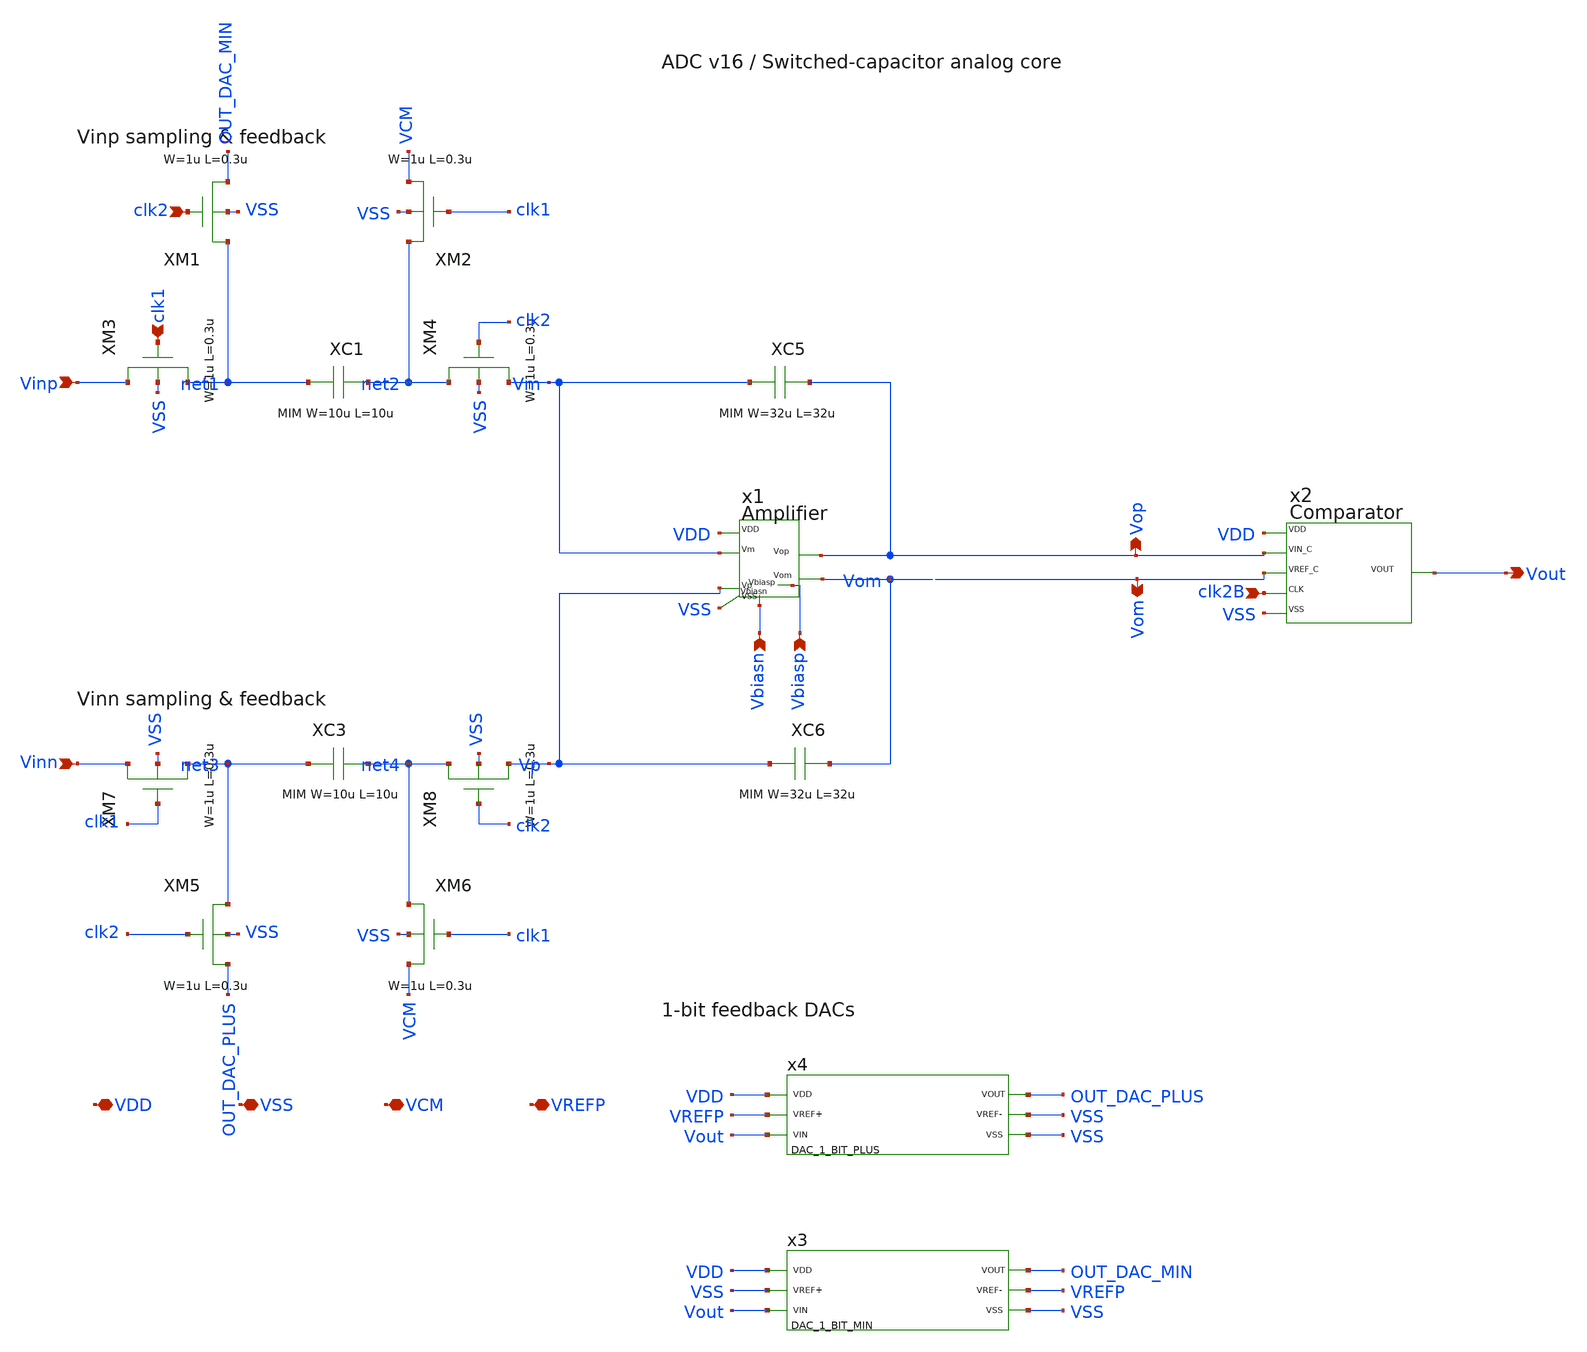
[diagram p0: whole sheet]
** sch_path: src/schematics/INTEGRATION/ADC_final/ADC_v17_Xschem/analog_integration_lvs.sch
* Copyright (C) 1998-2026 Stefan Frederik Schippers
* This program is free software; you can redistribute it and/or modify
* it under the terms of the GNU General Public License as published by
* the Free Software Foundation; either version 2 of the License, or
* (at your option) any later version.
**.subckt analog_integration_lvs Vinp Vinn Vop Vom clk1 clk2 Vbiasn Vbiasp clk2B Vout VDD VSS VCM
*+ VREFP
*.ipin Vinp
*.ipin Vinn
*.opin Vop
*.opin Vom
*.ipin clk1
*.ipin clk2
*.ipin Vbiasn
*.ipin Vbiasp
*.ipin clk2B
*.opin Vout
*.iopin VDD
*.iopin VSS
*.iopin VCM
*.iopin VREFP
XM1 net1 clk2 OUT_DAC_MIN VSS nfet_03v3 L=0.3u W=1u nf=1 ad='int((nf+1)/2) * W/nf * 0.18u' as='int((nf+2)/2) * W/nf * 0.18u'
+ pd='2*int((nf+1)/2) * (W/nf + 0.18u)' ps='2*int((nf+2)/2) * (W/nf + 0.18u)' nrd='0.18u / W' nrs='0.18u / W'
+ sa=0 sb=0 sd=0
XM2 net2 clk1 VCM VSS nfet_03v3 L=0.3u W=1u nf=1 ad='int((nf+1)/2) * W/nf * 0.18u' as='int((nf+2)/2) * W/nf * 0.18u'
+ pd='2*int((nf+1)/2) * (W/nf + 0.18u)' ps='2*int((nf+2)/2) * (W/nf + 0.18u)' nrd='0.18u / W' nrs='0.18u / W'
+ sa=0 sb=0 sd=0
XM3 Vinp clk1 net1 VSS nfet_03v3 L=0.3u W=1u nf=1 ad='int((nf+1)/2) * W/nf * 0.18u' as='int((nf+2)/2) * W/nf * 0.18u'
+ pd='2*int((nf+1)/2) * (W/nf + 0.18u)' ps='2*int((nf+2)/2) * (W/nf + 0.18u)' nrd='0.18u / W' nrs='0.18u / W'
+ sa=0 sb=0 sd=0
XM4 net2 clk2 Vm VSS nfet_03v3 L=0.3u W=1u nf=1 ad='int((nf+1)/2) * W/nf * 0.18u' as='int((nf+2)/2) * W/nf * 0.18u'
+ pd='2*int((nf+1)/2) * (W/nf + 0.18u)' ps='2*int((nf+2)/2) * (W/nf + 0.18u)' nrd='0.18u / W' nrs='0.18u / W'
+ sa=0 sb=0 sd=0
XM5 net3 clk2 OUT_DAC_PLUS VSS nfet_03v3 L=0.3u W=1u nf=1 ad='int((nf+1)/2) * W/nf * 0.18u' as='int((nf+2)/2) * W/nf * 0.18u'
+ pd='2*int((nf+1)/2) * (W/nf + 0.18u)' ps='2*int((nf+2)/2) * (W/nf + 0.18u)' nrd='0.18u / W' nrs='0.18u / W'
+ sa=0 sb=0 sd=0
XM6 net4 clk1 VCM VSS nfet_03v3 L=0.3u W=1u nf=1 ad='int((nf+1)/2) * W/nf * 0.18u' as='int((nf+2)/2) * W/nf * 0.18u'
+ pd='2*int((nf+1)/2) * (W/nf + 0.18u)' ps='2*int((nf+2)/2) * (W/nf + 0.18u)' nrd='0.18u / W' nrs='0.18u / W'
+ sa=0 sb=0 sd=0
XM7 Vinn clk1 net3 VSS nfet_03v3 L=0.3u W=1u nf=1 ad='int((nf+1)/2) * W/nf * 0.18u' as='int((nf+2)/2) * W/nf * 0.18u'
+ pd='2*int((nf+1)/2) * (W/nf + 0.18u)' ps='2*int((nf+2)/2) * (W/nf + 0.18u)' nrd='0.18u / W' nrs='0.18u / W'
+ sa=0 sb=0 sd=0
XM8 net4 clk2 Vp VSS nfet_03v3 L=0.3u W=1u nf=1 ad='int((nf+1)/2) * W/nf * 0.18u' as='int((nf+2)/2) * W/nf * 0.18u'
+ pd='2*int((nf+1)/2) * (W/nf + 0.18u)' ps='2*int((nf+2)/2) * (W/nf + 0.18u)' nrd='0.18u / W' nrs='0.18u / W'
+ sa=0 sb=0 sd=0
XC1 net2 net1 cap_mim_2f0_m4m5_noshield c_width=10u c_length=10u
XC3 net3 net4 cap_mim_2f0_m4m5_noshield c_width=10u c_length=10u
XC5 Vop Vm cap_mim_2f0_m4m5_noshield c_width=32u c_length=32u
XC6 Vom Vp cap_mim_2f0_m4m5_noshield c_width=32u c_length=32u
x1 VDD Vbiasp Vp Vop Vm Vom Vbiasn VSS fulldiffamp
x2 VDD Vop Vom clk2B Vout VSS ADCv16_verified_comparator
x4 VDD VREFP Vout OUT_DAC_PLUS VSS VSS DAC_1_BIT_PLUS
x3 VDD VSS Vout OUT_DAC_MIN VREFP VSS DAC_1_BIT_MIN
**.ends

* expanding   symbol:  ./fulldiffamp.sym # of pins=8
** sym_path: ./fulldiffamp.sym
** sch_path: ./fulldiffamp.sch
.subckt fulldiffamp VDD Vbiasp Vp Vop Vm Vom Vbiasn VSS
*.iopin VDD
*.iopin Vbiasp
*.iopin Vp
*.iopin Vop
*.iopin Vm
*.iopin Vom
*.iopin Vbiasn
*.iopin VSS
XM5 net2 Vom VDD VDD pfet_03v3 L=2u W=1u nf=1 ad='int((nf+1)/2) * W/nf * 0.18u' as='int((nf+2)/2) * W/nf * 0.18u'
+ pd='2*int((nf+1)/2) * (W/nf + 0.18u)' ps='2*int((nf+2)/2) * (W/nf + 0.18u)' nrd='0.18u / W' nrs='0.18u / W'
+ sa=0 sb=0 sd=0
XM2 Vom Vbiasp VDD VDD pfet_03v3 L=5u W=10u nf=1 ad='int((nf+1)/2) * W/nf * 0.18u' as='int((nf+2)/2) * W/nf * 0.18u'
+ pd='2*int((nf+1)/2) * (W/nf + 0.18u)' ps='2*int((nf+2)/2) * (W/nf + 0.18u)' nrd='0.18u / W' nrs='0.18u / W'
+ sa=0 sb=0 sd=0
XM8 Vom Vm net1 VSS nfet_03v3 L=5u W=10u nf=1 ad='int((nf+1)/2) * W/nf * 0.18u' as='int((nf+2)/2) * W/nf * 0.18u'
+ pd='2*int((nf+1)/2) * (W/nf + 0.18u)' ps='2*int((nf+2)/2) * (W/nf + 0.18u)' nrd='0.18u / W' nrs='0.18u / W'
+ sa=0 sb=0 sd=0
XM7 Vop Vp net1 VSS nfet_03v3 L=5u W=10u nf=1 ad='int((nf+1)/2) * W/nf * 0.18u' as='int((nf+2)/2) * W/nf * 0.18u'
+ pd='2*int((nf+1)/2) * (W/nf + 0.18u)' ps='2*int((nf+2)/2) * (W/nf + 0.18u)' nrd='0.18u / W' nrs='0.18u / W'
+ sa=0 sb=0 sd=0
XM1 Vop Vbiasp VDD VDD pfet_03v3 L=5u W=10u nf=1 ad='int((nf+1)/2) * W/nf * 0.18u' as='int((nf+2)/2) * W/nf * 0.18u'
+ pd='2*int((nf+1)/2) * (W/nf + 0.18u)' ps='2*int((nf+2)/2) * (W/nf + 0.18u)' nrd='0.18u / W' nrs='0.18u / W'
+ sa=0 sb=0 sd=0
XM6 net3 Vop VDD VDD pfet_03v3 L=2u W=1u nf=1 ad='int((nf+1)/2) * W/nf * 0.18u' as='int((nf+2)/2) * W/nf * 0.18u'
+ pd='2*int((nf+1)/2) * (W/nf + 0.18u)' ps='2*int((nf+2)/2) * (W/nf + 0.18u)' nrd='0.18u / W' nrs='0.18u / W'
+ sa=0 sb=0 sd=0
XM4 Vom VDD VDD VDD pfet_03v3 L=5u W=0.5u nf=1 ad='int((nf+1)/2) * W/nf * 0.18u' as='int((nf+2)/2) * W/nf * 0.18u'
+ pd='2*int((nf+1)/2) * (W/nf + 0.18u)' ps='2*int((nf+2)/2) * (W/nf + 0.18u)' nrd='0.18u / W' nrs='0.18u / W'
+ sa=0 sb=0 sd=0
XM3 Vop VDD VDD VDD pfet_03v3 L=5u W=0.5u nf=1 ad='int((nf+1)/2) * W/nf * 0.18u' as='int((nf+2)/2) * W/nf * 0.18u'
+ pd='2*int((nf+1)/2) * (W/nf + 0.18u)' ps='2*int((nf+2)/2) * (W/nf + 0.18u)' nrd='0.18u / W' nrs='0.18u / W'
+ sa=0 sb=0 sd=0
XM9 net1 Vbiasn VSS VSS nfet_03v3 L=2u W=10u nf=1 ad='int((nf+1)/2) * W/nf * 0.18u' as='int((nf+2)/2) * W/nf * 0.18u'
+ pd='2*int((nf+1)/2) * (W/nf + 0.18u)' ps='2*int((nf+2)/2) * (W/nf + 0.18u)' nrd='0.18u / W' nrs='0.18u / W'
+ sa=0 sb=0 sd=0
XM10 net1 Vbiasn VSS VSS nfet_03v3 L=2u W=10u nf=1 ad='int((nf+1)/2) * W/nf * 0.18u' as='int((nf+2)/2) * W/nf * 0.18u'
+ pd='2*int((nf+1)/2) * (W/nf + 0.18u)' ps='2*int((nf+2)/2) * (W/nf + 0.18u)' nrd='0.18u / W' nrs='0.18u / W'
+ sa=0 sb=0 sd=0
XM11 Vop net2 VSS VSS nfet_03v3 L=15u W=0.5u nf=1 ad='int((nf+1)/2) * W/nf * 0.18u' as='int((nf+2)/2) * W/nf * 0.18u'
+ pd='2*int((nf+1)/2) * (W/nf + 0.18u)' ps='2*int((nf+2)/2) * (W/nf + 0.18u)' nrd='0.18u / W' nrs='0.18u / W'
+ sa=0 sb=0 sd=0
XM13 net2 net2 VSS VSS nfet_03v3 L=0.35u W=5u nf=1 ad='int((nf+1)/2) * W/nf * 0.18u' as='int((nf+2)/2) * W/nf * 0.18u'
+ pd='2*int((nf+1)/2) * (W/nf + 0.18u)' ps='2*int((nf+2)/2) * (W/nf + 0.18u)' nrd='0.18u / W' nrs='0.18u / W'
+ sa=0 sb=0 sd=0
XM12 net3 net3 VSS VSS nfet_03v3 L=0.35u W=5u nf=1 ad='int((nf+1)/2) * W/nf * 0.18u' as='int((nf+2)/2) * W/nf * 0.18u'
+ pd='2*int((nf+1)/2) * (W/nf + 0.18u)' ps='2*int((nf+2)/2) * (W/nf + 0.18u)' nrd='0.18u / W' nrs='0.18u / W'
+ sa=0 sb=0 sd=0
XM14 Vom net3 VSS VSS nfet_03v3 L=15u W=0.5u nf=1 ad='int((nf+1)/2) * W/nf * 0.18u' as='int((nf+2)/2) * W/nf * 0.18u'
+ pd='2*int((nf+1)/2) * (W/nf + 0.18u)' ps='2*int((nf+2)/2) * (W/nf + 0.18u)' nrd='0.18u / W' nrs='0.18u / W'
+ sa=0 sb=0 sd=0
.ends


* expanding   symbol:  ./ADCv16_verified_comparator.sym # of pins=6
** sym_path: ./ADCv16_verified_comparator.sym
** sch_path: ./ADCv16_verified_comparator.sch
.subckt ADCv16_verified_comparator VDD VIN_C VREF_C CLK VOUT VSS
*.iopin VDD
*.iopin VIN_C
*.iopin VREF_C
*.iopin CLK
*.iopin VOUT
*.iopin VSS
XM1 net3 VIN_C net1 VDD pfet_03v3 L=0.3u W=5u nf=1 ad='int((nf+1)/2) * W/nf * 0.18u' as='int((nf+2)/2) * W/nf * 0.18u'
+ pd='2*int((nf+1)/2) * (W/nf + 0.18u)' ps='2*int((nf+2)/2) * (W/nf + 0.18u)' nrd='0.18u / W' nrs='0.18u / W'
+ sa=0 sb=0 sd=0
XM2 net5 VREF_C net1 VDD pfet_03v3 L=0.3u W=5u nf=1 ad='int((nf+1)/2) * W/nf * 0.18u' as='int((nf+2)/2) * W/nf * 0.18u'
+ pd='2*int((nf+1)/2) * (W/nf + 0.18u)' ps='2*int((nf+2)/2) * (W/nf + 0.18u)' nrd='0.18u / W' nrs='0.18u / W'
+ sa=0 sb=0 sd=0
XM3 VOUT net2 net5 VDD pfet_03v3 L=0.3u W=5u nf=1 ad='int((nf+1)/2) * W/nf * 0.18u' as='int((nf+2)/2) * W/nf * 0.18u'
+ pd='2*int((nf+1)/2) * (W/nf + 0.18u)' ps='2*int((nf+2)/2) * (W/nf + 0.18u)' nrd='0.18u / W' nrs='0.18u / W'
+ sa=0 sb=0 sd=0
XM4 net4 net2 net3 VDD pfet_03v3 L=0.3u W=5u nf=1 ad='int((nf+1)/2) * W/nf * 0.18u' as='int((nf+2)/2) * W/nf * 0.18u'
+ pd='2*int((nf+1)/2) * (W/nf + 0.18u)' ps='2*int((nf+2)/2) * (W/nf + 0.18u)' nrd='0.18u / W' nrs='0.18u / W'
+ sa=0 sb=0 sd=0
XM6 net2 CLK VDD VDD pfet_03v3 L=0.3u W=5u nf=1 ad='int((nf+1)/2) * W/nf * 0.18u' as='int((nf+2)/2) * W/nf * 0.18u'
+ pd='2*int((nf+1)/2) * (W/nf + 0.18u)' ps='2*int((nf+2)/2) * (W/nf + 0.18u)' nrd='0.18u / W' nrs='0.18u / W'
+ sa=0 sb=0 sd=0
XM7 net2 CLK VSS VSS nfet_03v3 L=0.3u W=2.5u nf=1 ad='int((nf+1)/2) * W/nf * 0.18u' as='int((nf+2)/2) * W/nf * 0.18u'
+ pd='2*int((nf+1)/2) * (W/nf + 0.18u)' ps='2*int((nf+2)/2) * (W/nf + 0.18u)' nrd='0.18u / W' nrs='0.18u / W'
+ sa=0 sb=0 sd=0
XM8 net4 CLK VOUT VSS nfet_03v3 L=0.3u W=2.5u nf=1 ad='int((nf+1)/2) * W/nf * 0.18u' as='int((nf+2)/2) * W/nf * 0.18u'
+ pd='2*int((nf+1)/2) * (W/nf + 0.18u)' ps='2*int((nf+2)/2) * (W/nf + 0.18u)' nrd='0.18u / W' nrs='0.18u / W'
+ sa=0 sb=0 sd=0
XM9 net7 VOUT VDD VDD pfet_03v3 L=0.3u W=5u nf=1 ad='int((nf+1)/2) * W/nf * 0.18u' as='int((nf+2)/2) * W/nf * 0.18u'
+ pd='2*int((nf+1)/2) * (W/nf + 0.18u)' ps='2*int((nf+2)/2) * (W/nf + 0.18u)' nrd='0.18u / W' nrs='0.18u / W'
+ sa=0 sb=0 sd=0
XM10 net4 CLK net7 VDD pfet_03v3 L=0.3u W=5u nf=1 ad='int((nf+1)/2) * W/nf * 0.18u' as='int((nf+2)/2) * W/nf * 0.18u'
+ pd='2*int((nf+1)/2) * (W/nf + 0.18u)' ps='2*int((nf+2)/2) * (W/nf + 0.18u)' nrd='0.18u / W' nrs='0.18u / W'
+ sa=0 sb=0 sd=0
XM11 net4 VOUT VSS VSS nfet_03v3 L=0.3u W=2.5u nf=1 ad='int((nf+1)/2) * W/nf * 0.18u' as='int((nf+2)/2) * W/nf * 0.18u'
+ pd='2*int((nf+1)/2) * (W/nf + 0.18u)' ps='2*int((nf+2)/2) * (W/nf + 0.18u)' nrd='0.18u / W' nrs='0.18u / W'
+ sa=0 sb=0 sd=0
XM12 net6 net4 VDD VDD pfet_03v3 L=0.3u W=5u nf=1 ad='int((nf+1)/2) * W/nf * 0.18u' as='int((nf+2)/2) * W/nf * 0.18u'
+ pd='2*int((nf+1)/2) * (W/nf + 0.18u)' ps='2*int((nf+2)/2) * (W/nf + 0.18u)' nrd='0.18u / W' nrs='0.18u / W'
+ sa=0 sb=0 sd=0
XM13 VOUT CLK net6 VDD pfet_03v3 L=0.3u W=5u nf=1 ad='int((nf+1)/2) * W/nf * 0.18u' as='int((nf+2)/2) * W/nf * 0.18u'
+ pd='2*int((nf+1)/2) * (W/nf + 0.18u)' ps='2*int((nf+2)/2) * (W/nf + 0.18u)' nrd='0.18u / W' nrs='0.18u / W'
+ sa=0 sb=0 sd=0
XM14 VOUT net4 VSS VSS nfet_03v3 L=0.3u W=2.5u nf=1 ad='int((nf+1)/2) * W/nf * 0.18u' as='int((nf+2)/2) * W/nf * 0.18u'
+ pd='2*int((nf+1)/2) * (W/nf + 0.18u)' ps='2*int((nf+2)/2) * (W/nf + 0.18u)' nrd='0.18u / W' nrs='0.18u / W'
+ sa=0 sb=0 sd=0
XM5 net1 VSS VDD VDD pfet_03v3 L=0.3u W=10u nf=1 ad='int((nf+1)/2) * W/nf * 0.18u' as='int((nf+2)/2) * W/nf * 0.18u'
+ pd='2*int((nf+1)/2) * (W/nf + 0.18u)' ps='2*int((nf+2)/2) * (W/nf + 0.18u)' nrd='0.18u / W' nrs='0.18u / W'
+ sa=0 sb=0 sd=0
.ends


* expanding   symbol:  ./DAC_1_BIT_PLUS.sym # of pins=6
** sym_path: ./DAC_1_BIT_PLUS.sym
** sch_path: ./DAC_1_BIT_PLUS.sch
.subckt DAC_1_BIT_PLUS VDD VREF+ VIN VOUT VREF- VSS
*.iopin VDD
*.iopin VREF+
*.iopin VIN
*.iopin VOUT
*.iopin VREF-
*.iopin VSS
XM1 net1 net2 VREF+ VSS nfet_03v3 L=Ld W=Wdn_p nf=2 ad='int((nf+1)/2) * W/nf * 0.18u' as='int((nf+2)/2) * W/nf * 0.18u'
+ pd='2*int((nf+1)/2) * (W/nf + 0.18u)' ps='2*int((nf+2)/2) * (W/nf + 0.18u)' nrd='0.18u / W' nrs='0.18u / W'
+ sa=0 sb=0 sd=0
XM2 net1 VIN VREF+ VDD pfet_03v3 L=Ld W=Wdp_p nf=2 ad='int((nf+1)/2) * W/nf * 0.18u' as='int((nf+2)/2) * W/nf * 0.18u'
+ pd='2*int((nf+1)/2) * (W/nf + 0.18u)' ps='2*int((nf+2)/2) * (W/nf + 0.18u)' nrd='0.18u / W' nrs='0.18u / W'
+ sa=0 sb=0 sd=0
XM3 net1 VIN VREF- VSS nfet_03v3 L=Ld W=Wdn_p nf=2 ad='int((nf+1)/2) * W/nf * 0.18u' as='int((nf+2)/2) * W/nf * 0.18u'
+ pd='2*int((nf+1)/2) * (W/nf + 0.18u)' ps='2*int((nf+2)/2) * (W/nf + 0.18u)' nrd='0.18u / W' nrs='0.18u / W'
+ sa=0 sb=0 sd=0
XM4 net1 net2 VREF- VDD pfet_03v3 L=Ld W=Wdp_p nf=2 ad='int((nf+1)/2) * W/nf * 0.18u' as='int((nf+2)/2) * W/nf * 0.18u'
+ pd='2*int((nf+1)/2) * (W/nf + 0.18u)' ps='2*int((nf+2)/2) * (W/nf + 0.18u)' nrd='0.18u / W' nrs='0.18u / W'
+ sa=0 sb=0 sd=0
XM5 net2 VIN VDD VDD pfet_03v3 L=Ld W=Wsp_p nf=1 ad='int((nf+1)/2) * W/nf * 0.18u' as='int((nf+2)/2) * W/nf * 0.18u'
+ pd='2*int((nf+1)/2) * (W/nf + 0.18u)' ps='2*int((nf+2)/2) * (W/nf + 0.18u)' nrd='0.18u / W' nrs='0.18u / W'
+ sa=0 sb=0 sd=0
XM6 net2 VIN VSS VSS nfet_03v3 L=Ld W=Wsn_p nf=1 ad='int((nf+1)/2) * W/nf * 0.18u' as='int((nf+2)/2) * W/nf * 0.18u'
+ pd='2*int((nf+1)/2) * (W/nf + 0.18u)' ps='2*int((nf+2)/2) * (W/nf + 0.18u)' nrd='0.18u / W' nrs='0.18u / W'
+ sa=0 sb=0 sd=0
XM7 net3 net1 VDD VDD pfet_03v3 L=Ld W=Wsp_p nf=1 ad='int((nf+1)/2) * W/nf * 0.18u' as='int((nf+2)/2) * W/nf * 0.18u'
+ pd='2*int((nf+1)/2) * (W/nf + 0.18u)' ps='2*int((nf+2)/2) * (W/nf + 0.18u)' nrd='0.18u / W' nrs='0.18u / W'
+ sa=0 sb=0 sd=0
XM8 net3 net1 VSS VSS nfet_03v3 L=Ld W=Wsn_p nf=1 ad='int((nf+1)/2) * W/nf * 0.18u' as='int((nf+2)/2) * W/nf * 0.18u'
+ pd='2*int((nf+1)/2) * (W/nf + 0.18u)' ps='2*int((nf+2)/2) * (W/nf + 0.18u)' nrd='0.18u / W' nrs='0.18u / W'
+ sa=0 sb=0 sd=0
XM9 VOUT net3 VDD VDD pfet_03v3 L=Ld W=Wsp2_p nf=1 ad='int((nf+1)/2) * W/nf * 0.18u' as='int((nf+2)/2) * W/nf * 0.18u'
+ pd='2*int((nf+1)/2) * (W/nf + 0.18u)' ps='2*int((nf+2)/2) * (W/nf + 0.18u)' nrd='0.18u / W' nrs='0.18u / W'
+ sa=0 sb=0 sd=0
XM10 VOUT net3 VSS VSS nfet_03v3 L=Ld W=Wsn2_p nf=1 ad='int((nf+1)/2) * W/nf * 0.18u' as='int((nf+2)/2) * W/nf * 0.18u'
+ pd='2*int((nf+1)/2) * (W/nf + 0.18u)' ps='2*int((nf+2)/2) * (W/nf + 0.18u)' nrd='0.18u / W' nrs='0.18u / W'
+ sa=0 sb=0 sd=0
.ends


* expanding   symbol:  ./DAC_1_BIT_MIN.sym # of pins=6
** sym_path: ./DAC_1_BIT_MIN.sym
** sch_path: ./DAC_1_BIT_MIN.sch
.subckt DAC_1_BIT_MIN VDD VREF+ VIN VOUT VREF- VSS
*.iopin VDD
*.iopin VREF+
*.iopin VIN
*.iopin VOUT
*.iopin VREF-
*.iopin VSS
XM1 net1 net2 VREF+ VSS nfet_03v3 L=0.28u W=1u nf=2 ad='int((nf+1)/2) * W/nf * 0.18u' as='int((nf+2)/2) * W/nf * 0.18u'
+ pd='2*int((nf+1)/2) * (W/nf + 0.18u)' ps='2*int((nf+2)/2) * (W/nf + 0.18u)' nrd='0.18u / W' nrs='0.18u / W'
+ sa=0 sb=0 sd=0
XM2 net1 VIN VREF+ VDD pfet_03v3 L=0.28u W=10u nf=2 ad='int((nf+1)/2) * W/nf * 0.18u' as='int((nf+2)/2) * W/nf * 0.18u'
+ pd='2*int((nf+1)/2) * (W/nf + 0.18u)' ps='2*int((nf+2)/2) * (W/nf + 0.18u)' nrd='0.18u / W' nrs='0.18u / W'
+ sa=0 sb=0 sd=0
XM3 net1 VIN VREF- VSS nfet_03v3 L=0.28u W=1u nf=2 ad='int((nf+1)/2) * W/nf * 0.18u' as='int((nf+2)/2) * W/nf * 0.18u'
+ pd='2*int((nf+1)/2) * (W/nf + 0.18u)' ps='2*int((nf+2)/2) * (W/nf + 0.18u)' nrd='0.18u / W' nrs='0.18u / W'
+ sa=0 sb=0 sd=0
XM4 net1 net2 VREF- VDD pfet_03v3 L=0.28u W=10u nf=2 ad='int((nf+1)/2) * W/nf * 0.18u' as='int((nf+2)/2) * W/nf * 0.18u'
+ pd='2*int((nf+1)/2) * (W/nf + 0.18u)' ps='2*int((nf+2)/2) * (W/nf + 0.18u)' nrd='0.18u / W' nrs='0.18u / W'
+ sa=0 sb=0 sd=0
XM5 net2 VIN VDD VDD pfet_03v3 L=0.28u W=5u nf=1 ad='int((nf+1)/2) * W/nf * 0.18u' as='int((nf+2)/2) * W/nf * 0.18u'
+ pd='2*int((nf+1)/2) * (W/nf + 0.18u)' ps='2*int((nf+2)/2) * (W/nf + 0.18u)' nrd='0.18u / W' nrs='0.18u / W'
+ sa=0 sb=0 sd=0
XM6 net2 VIN VSS VSS nfet_03v3 L=0.28u W=0.5u nf=1 ad='int((nf+1)/2) * W/nf * 0.18u' as='int((nf+2)/2) * W/nf * 0.18u'
+ pd='2*int((nf+1)/2) * (W/nf + 0.18u)' ps='2*int((nf+2)/2) * (W/nf + 0.18u)' nrd='0.18u / W' nrs='0.18u / W'
+ sa=0 sb=0 sd=0
XM7 VOUT net1 VDD VDD pfet_03v3 L=0.28u W=5u nf=1 ad='int((nf+1)/2) * W/nf * 0.18u' as='int((nf+2)/2) * W/nf * 0.18u'
+ pd='2*int((nf+1)/2) * (W/nf + 0.18u)' ps='2*int((nf+2)/2) * (W/nf + 0.18u)' nrd='0.18u / W' nrs='0.18u / W'
+ sa=0 sb=0 sd=0
XM8 VOUT net1 VSS VSS nfet_03v3 L=0.28u W=0.5u nf=1 ad='int((nf+1)/2) * W/nf * 0.18u' as='int((nf+2)/2) * W/nf * 0.18u'
+ pd='2*int((nf+1)/2) * (W/nf + 0.18u)' ps='2*int((nf+2)/2) * (W/nf + 0.18u)' nrd='0.18u / W' nrs='0.18u / W'
+ sa=0 sb=0 sd=0
.ends

.end
